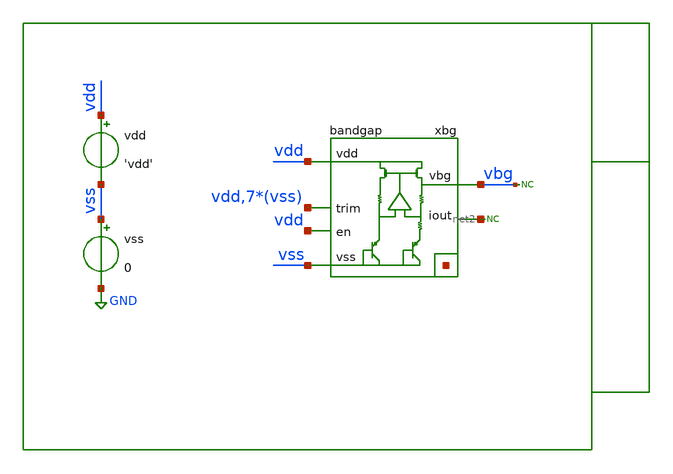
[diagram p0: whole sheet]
** sch_path: xschem/tb/bandgap_cm/bandgap/dc_bandgap_power.sch
**.subckt dc_bandgap_power
xbg vdd vbg vss net1[7] net1[6] net1[5] net1[4] net1[3] net1[2] net1[1] net1[0] vdd vss vss vss vss
+ vss vss vss net2 vdd bandgap
vdd vdd vss 'vdd'
vss vss GND 0
* noconn vbg
* noconn #net2
**** begin user architecture code

* Control

.param vdd = 3.3
.temp 27

.options reltol     = 1e-6

*------------------------------------------------------------
* Nodeset for better convergence
*------------------------------------------------------------
.nodeset v(vbg)  = '1'
.nodeset v(xbg.gate) = 'vdd/2'
.nodeset v(xbg.vx)   = '0.70'
.nodeset v(xbg.vbe2) = '0.65'
.nodeset v(xbg.vs1)  = '0'
*------------------------------------------------------------

*------------------------------------------------------------
* Save device current for DC analysis
*------------------------------------------------------------
.save @m.xbg.xm1.m0[id]
.save @m.xbg.xm2.m0[id]
.save @m.xbg.xamp.xmb1.m0[id]
.save @m.xbg.xamp.xmb2.m0[id]
.save @m.xbg.xamp.xmt1.m0[id]
.save @m.xbg.xamp.xmc7.m0[id]
.save @m.xbg.xamp.xmc8.m0[id]

.control
save all

*optran 0 0 0 100n 0.1m 0

dc vdd  2.5 5 0.1

let vsup = v(vdd)

let itot = abs(vdd#branch)

let id_xm1  = abs(@m.xbg.xm1.m0[id])
let id_xm2  = abs(@m.xbg.xm2.m0[id])
let id_xmb1 = abs(@m.xbg.xamp.xmb1.m0[id])
let id_xmb2 = abs(@m.xbg.xamp.xmb2.m0[id])
let id_xmt1 = abs(@m.xbg.xamp.xmt1.m0[id])
let id_xmc7 = abs(@m.xbg.xamp.xmc7.m0[id])
let id_xmc8 = abs(@m.xbg.xamp.xmc8.m0[id])

let iamp = id_xmb1 + id_xmb2 + id_xmt1 + id_xmc7 + id_xmc8
let ibgc = id_xm1 + id_xm2
let isum = iamp + ibgc

let pamp = vsup*iamp
let pbgc = vsup*ibgc
let psum = vsup*isum
let ptot = vsup*itot

gnuplot p1 itot isum iamp ibgc
gnuplot p2 ptot psum pamp pbgc

meas dc i_min min itot from=2.5 to=5
meas dc i_max max itot from=2.5 to=5
meas dc p_min min ptot from=2.5 to=5
meas dc p_max max ptot from=2.5 to=5

print i_min
print i_max
print p_min
print p_max


.endc
.end


 * Model Corners

.include $::CORNERS/ngspice/tt.spice
*.include $::CORNERS/ngspice/ff.spice
*.include $::CORNERS/ngspice/ss.spice
*.include $::CORNERS/ngspice/sf.spice
*.include $::CORNERS/ngspice/fs.spice

**** end user architecture code
**.ends
.GLOBAL GND
.end
